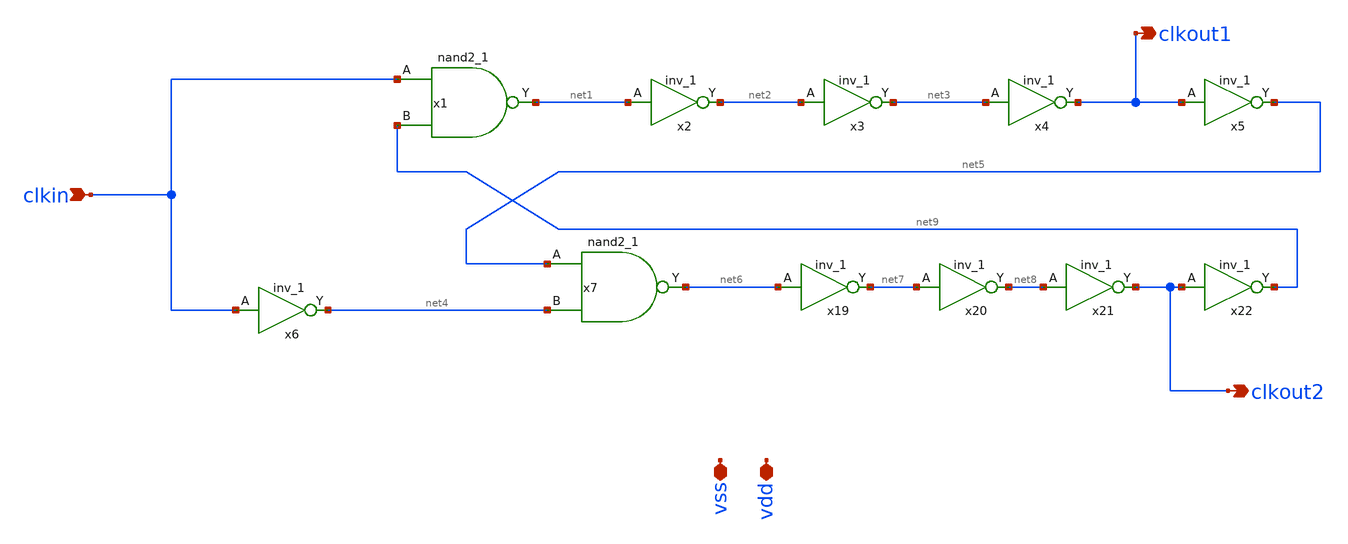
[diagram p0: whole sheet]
** sch_path: Clock_generator.sch
**.subckt Clock_generator clkin clkout1 clkout2 vss vdd
*.ipin clkin
*.opin clkout1
*.opin clkout2
*.iopin vss
*.iopin vdd
x1 clkin net9 vss vss vdd vdd net1 sky130_fd_sc_hd__nand2_1
x2 net1 vss vss vdd vdd net2 sky130_fd_sc_hd__inv_1
x3 net2 vss vss vdd vdd net3 sky130_fd_sc_hd__inv_1
x4 net3 vss vss vdd vdd clkout1 sky130_fd_sc_hd__inv_1
x5 clkout1 vss vss vdd vdd net5 sky130_fd_sc_hd__inv_1
x6 clkin vss vss vdd vdd net4 sky130_fd_sc_hd__inv_1
x7 net5 net4 vss vss vdd vdd net6 sky130_fd_sc_hd__nand2_1
x19 net6 vss vss vdd vdd net7 sky130_fd_sc_hd__inv_1
x20 net7 vss vss vdd vdd net8 sky130_fd_sc_hd__inv_1
x21 net8 vss vss vdd vdd clkout2 sky130_fd_sc_hd__inv_1
x22 clkout2 vss vss vdd vdd net9 sky130_fd_sc_hd__inv_1
**.ends
.end
